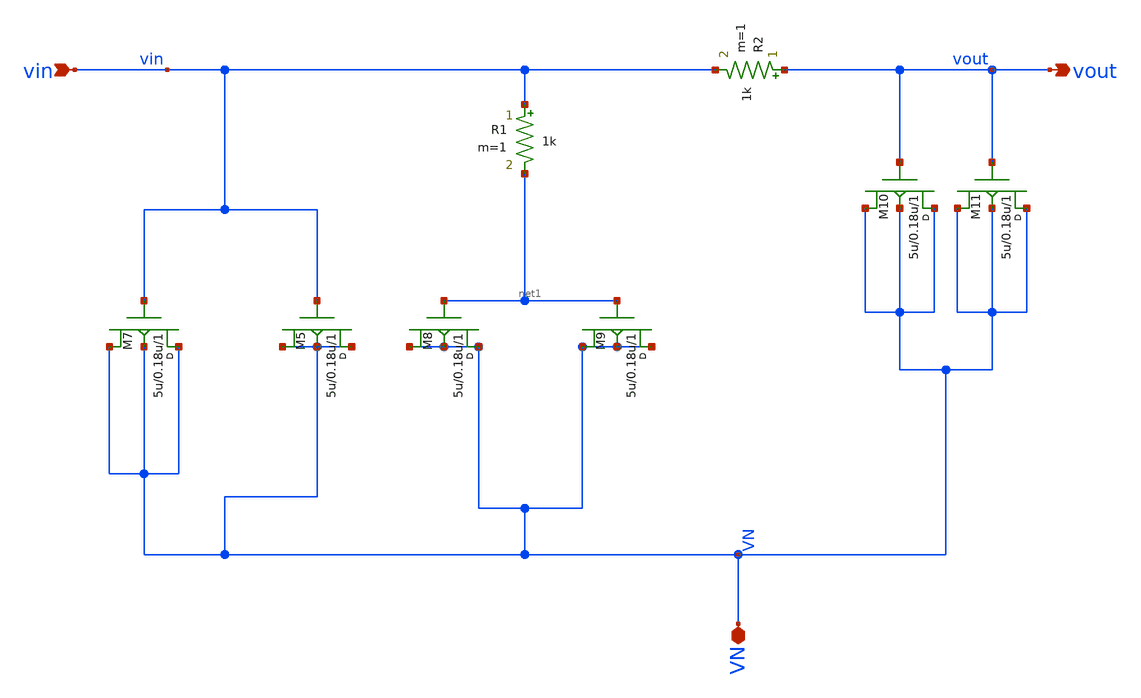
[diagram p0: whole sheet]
** sch_path: git_11/LOOP_FILTER.sch
**.subckt LOOP_FILTER VN vin vout
*.iopin VN
*.ipin vin
*.opin vout
M7 VN vin VN VN nmos w=5u l=0.18u m=1
M5 VN vin VN VN nmos w=5u l=0.18u m=1
M8 VN net1 VN VN nmos w=5u l=0.18u m=1
M9 VN net1 VN VN nmos w=5u l=0.18u m=1
M10 VN vout VN VN nmos w=5u l=0.18u m=1
M11 VN vout VN VN nmos w=5u l=0.18u m=1
R1 vin net1 1k m=1
R2 vout vin 1k m=1
**.ends
.end
